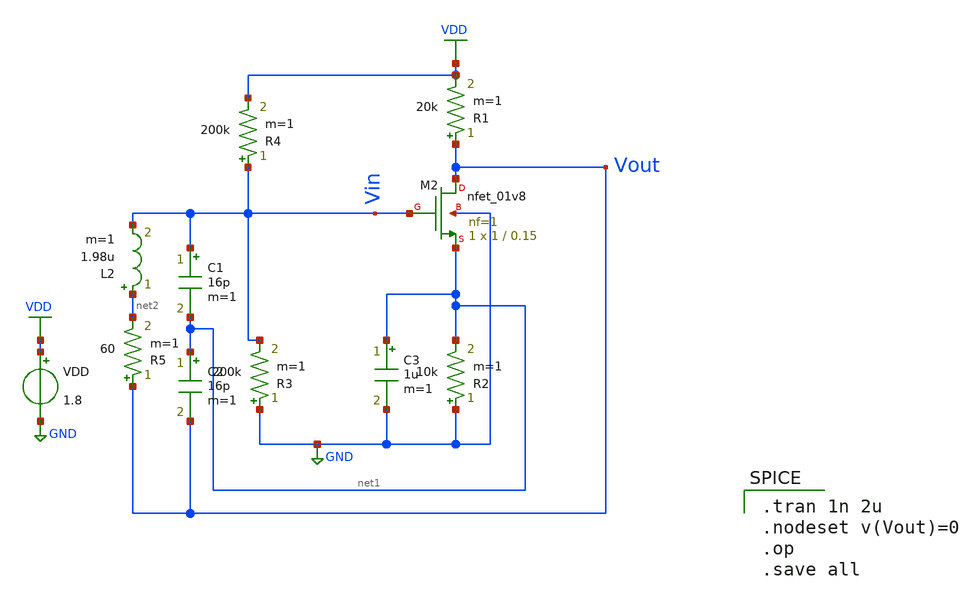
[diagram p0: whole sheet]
** sch_path: pll/xctl_lib/xctl/xschem/schematic_crystal_v2.sch
**.subckt schematic_crystal_v2
VDD VDD GND 1.8
XM2 Vout Vin net1 GND sky130_fd_pr__nfet_01v8 L=0.15 W=1 nf=1 ad='int((nf+1)/2) * W/nf * 0.29' as='int((nf+2)/2) * W/nf * 0.29'
+ pd='2*int((nf+1)/2) * (W/nf + 0.29)' ps='2*int((nf+2)/2) * (W/nf + 0.29)' nrd='0.29 / W' nrs='0.29 / W'
+ sa=0 sb=0 sd=0 mult=1 m=1
R2 GND net1 10k m=1
R3 GND Vin 200k m=1
R4 Vin VDD 200k m=1
L2 net2 Vin 1.98u m=1
R5 Vout net2 60 m=1
R1 Vout VDD 20k m=1
C1 Vin net1 16p m=1
C2 net1 Vout 16p m=1
C3 net1 GND 1u m=1
**** begin user architecture code

.tran 1n 2u
.nodeset v(Vout)=0
.op
.save all


** opencircuitdesign pdks install
.lib $::SKYWATER_MODELS/sky130.lib.spice tt


**** end user architecture code
**.ends
.GLOBAL GND
.GLOBAL VDD
.end
